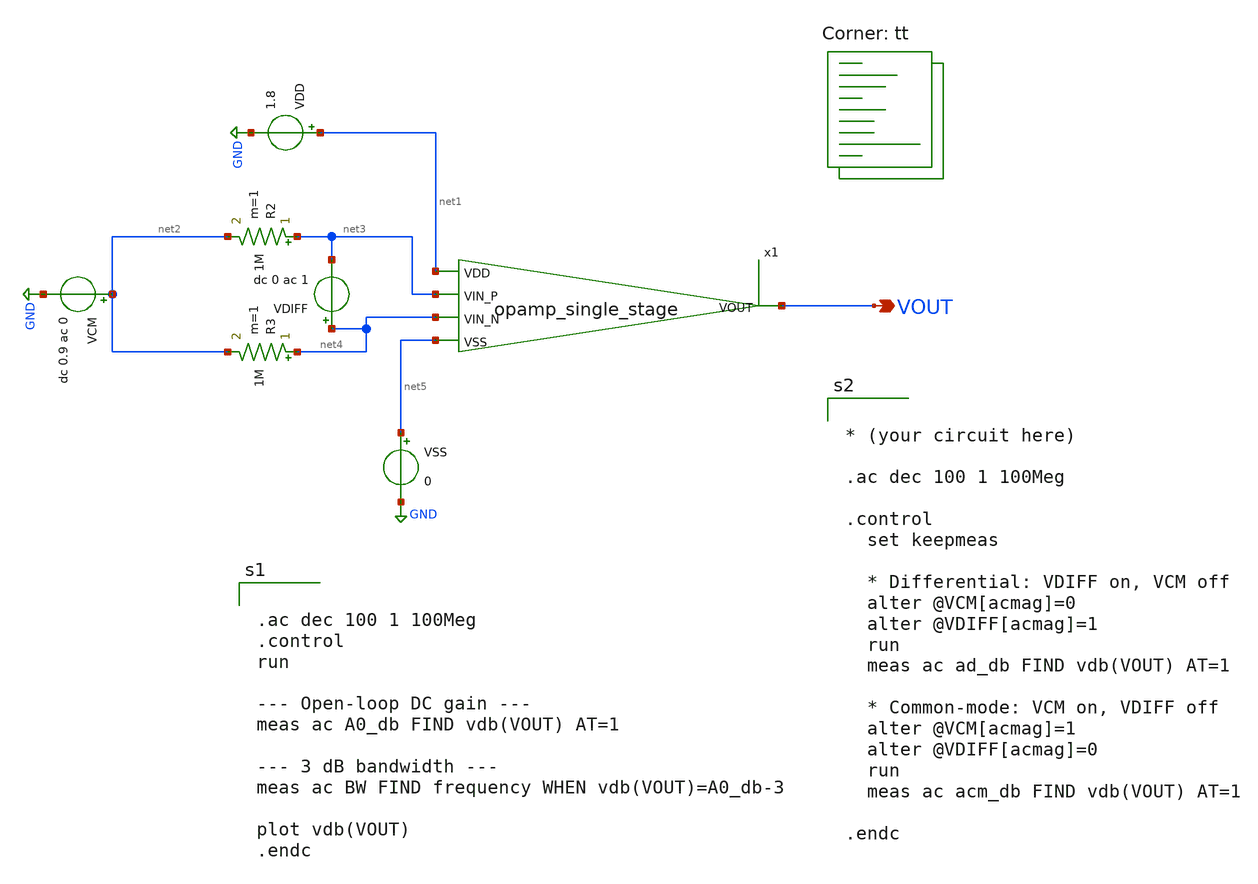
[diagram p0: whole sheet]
** sch_path: analog/schematics/testbenches/tb_ac_analysis.sch
**.subckt tb_ac_analysis VOUT
*.opin VOUT
VDD net1 GND 1.8
VSS net5 GND 0
VCM net2 GND dc 0.9 ac 0
R2 net3 net2 1M m=1
R3 net4 net2 1M m=1
VDIFF net4 net3 dc 0 ac 1
x1 net1 VOUT net3 net4 net5 opamp_single_stage
**** begin user architecture code
.lib $::SKYWATER_MODELS/sky130.lib.spice tt


* (your circuit here)

.ac dec 100 1 100Meg

.control
  set keepmeas

  * Differential: VDIFF on, VCM off
  alter @VCM[acmag]=0
  alter @VDIFF[acmag]=1
  run
  meas ac ad_db FIND vdb(VOUT) AT=1

  * Common-mode: VCM on, VDIFF off
  alter @VCM[acmag]=1
  alter @VDIFF[acmag]=0
  run
  meas ac acm_db FIND vdb(VOUT) AT=1

.endc




.ac dec 100 1 100Meg
.control
run

--- Open-loop DC gain ---
meas ac A0_db FIND vdb(VOUT) AT=1

--- 3 dB bandwidth ---
meas ac BW FIND frequency WHEN vdb(VOUT)=A0_db-3

plot vdb(VOUT)
.endc


**** end user architecture code
**.ends

* expanding   symbol:  opamp_single_stage.sym # of pins=5
** sym_path: analog/schematics/opamp_single_stage.sym
** sch_path: analog/schematics/opamp_single_stage.sch
.subckt opamp_single_stage VDD VOUT VIN_P VIN_N VSS
*.ipin VDD
*.ipin VIN_P
*.ipin VSS
*.opin VOUT
*.ipin VIN_N
XM4 net2 net1 VDD VDD sky130_fd_pr__pfet_01v8 L=0.5 W=8 nf=1 ad='int((nf+1)/2) * W/nf * 0.29' as='int((nf+2)/2) * W/nf * 0.29'
+ pd='2*int((nf+1)/2) * (W/nf + 0.29)' ps='2*int((nf+2)/2) * (W/nf + 0.29)' nrd='0.29 / W' nrs='0.29 / W'
+ sa=0 sb=0 sd=0 mult=1 m=1
XM3 net1 net1 VDD VDD sky130_fd_pr__pfet_01v8 L=0.5 W=8 nf=1 ad='int((nf+1)/2) * W/nf * 0.29' as='int((nf+2)/2) * W/nf * 0.29'
+ pd='2*int((nf+1)/2) * (W/nf + 0.29)' ps='2*int((nf+2)/2) * (W/nf + 0.29)' nrd='0.29 / W' nrs='0.29 / W'
+ sa=0 sb=0 sd=0 mult=1 m=1
XM1 net1 VIN_N net3 GND sky130_fd_pr__nfet_01v8_lvt L=0.5 W=6 nf=1 ad='int((nf+1)/2) * W/nf * 0.29' as='int((nf+2)/2) * W/nf * 0.29'
+ pd='2*int((nf+1)/2) * (W/nf + 0.29)' ps='2*int((nf+2)/2) * (W/nf + 0.29)' nrd='0.29 / W' nrs='0.29 / W'
+ sa=0 sb=0 sd=0 mult=1 m=1
XM2 net2 VIN_P net3 GND sky130_fd_pr__nfet_01v8_lvt L=0.5 W=6 nf=1 ad='int((nf+1)/2) * W/nf * 0.29' as='int((nf+2)/2) * W/nf * 0.29'
+ pd='2*int((nf+1)/2) * (W/nf + 0.29)' ps='2*int((nf+2)/2) * (W/nf + 0.29)' nrd='0.29 / W' nrs='0.29 / W'
+ sa=0 sb=0 sd=0 mult=1 m=1
XM5 VOUT net2 VDD VDD sky130_fd_pr__pfet_01v8 L=0.5 W=20 nf=1 ad='int((nf+1)/2) * W/nf * 0.29' as='int((nf+2)/2) * W/nf * 0.29'
+ pd='2*int((nf+1)/2) * (W/nf + 0.29)' ps='2*int((nf+2)/2) * (W/nf + 0.29)' nrd='0.29 / W' nrs='0.29 / W'
+ sa=0 sb=0 sd=0 mult=1 m=1
XC1 net5 VOUT sky130_fd_pr__cap_mim_m3_1 W=25 L=20 MF=1 m=1
XM8 net4 net4 VSS VSS sky130_fd_pr__nfet_01v8_lvt L=1.0 W=2 nf=1 ad='int((nf+1)/2) * W/nf * 0.29' as='int((nf+2)/2) * W/nf * 0.29'
+ pd='2*int((nf+1)/2) * (W/nf + 0.29)' ps='2*int((nf+2)/2) * (W/nf + 0.29)' nrd='0.29 / W' nrs='0.29 / W'
+ sa=0 sb=0 sd=0 mult=1 m=1
XM7 net3 net4 VSS VSS sky130_fd_pr__nfet_01v8_lvt L=1.0 W=4 nf=1 ad='int((nf+1)/2) * W/nf * 0.29' as='int((nf+2)/2) * W/nf * 0.29'
+ pd='2*int((nf+1)/2) * (W/nf + 0.29)' ps='2*int((nf+2)/2) * (W/nf + 0.29)' nrd='0.29 / W' nrs='0.29 / W'
+ sa=0 sb=0 sd=0 mult=1 m=1
XM6 VOUT net4 VSS VSS sky130_fd_pr__nfet_01v8_lvt L=1.0 W=8 nf=1 ad='int((nf+1)/2) * W/nf * 0.29' as='int((nf+2)/2) * W/nf * 0.29'
+ pd='2*int((nf+1)/2) * (W/nf + 0.29)' ps='2*int((nf+2)/2) * (W/nf + 0.29)' nrd='0.29 / W' nrs='0.29 / W'
+ sa=0 sb=0 sd=0 mult=1 m=1
R1 net5 net2 7k m=1
XR2 net4 VDD VDD sky130_fd_pr__res_high_po W=0.35 L=14 mult=1 m=1
.ends

.GLOBAL GND
.end
